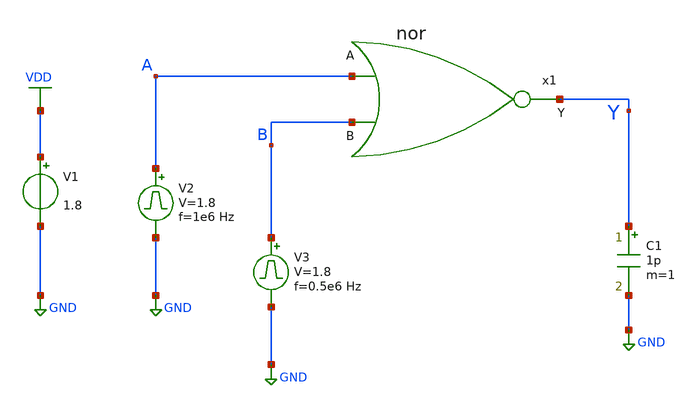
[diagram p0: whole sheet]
** sch_path: xschem/nor_tb.sch
**.subckt nor_tb
V1 VDD GND 1.8
V2 A GND pulse 0 1.8 '0.495/ 1e6 ' '0.01/1e6 ' '0.01/1e6 ' '0.49/1e6 ' '1/1e6 '
C1 Y GND 1p m=1
V3 B GND pulse 0 1.8 '0.495/ 0.5e6 ' '0.01/0.5e6 ' '0.01/0.5e6 ' '0.49/0.5e6 ' '1/0.5e6 '
x1 Y A B nor
**** begin user architecture code


.control
save all
tran 1n 2u
plot V(A) V(B)+2 V(Y)+4
.endc



** opencircuitdesign pdks install
.lib $::SKYWATER_MODELS/sky130.lib.spice tt


**** end user architecture code
**.ends
.GLOBAL VDD
.GLOBAL GND
.end
